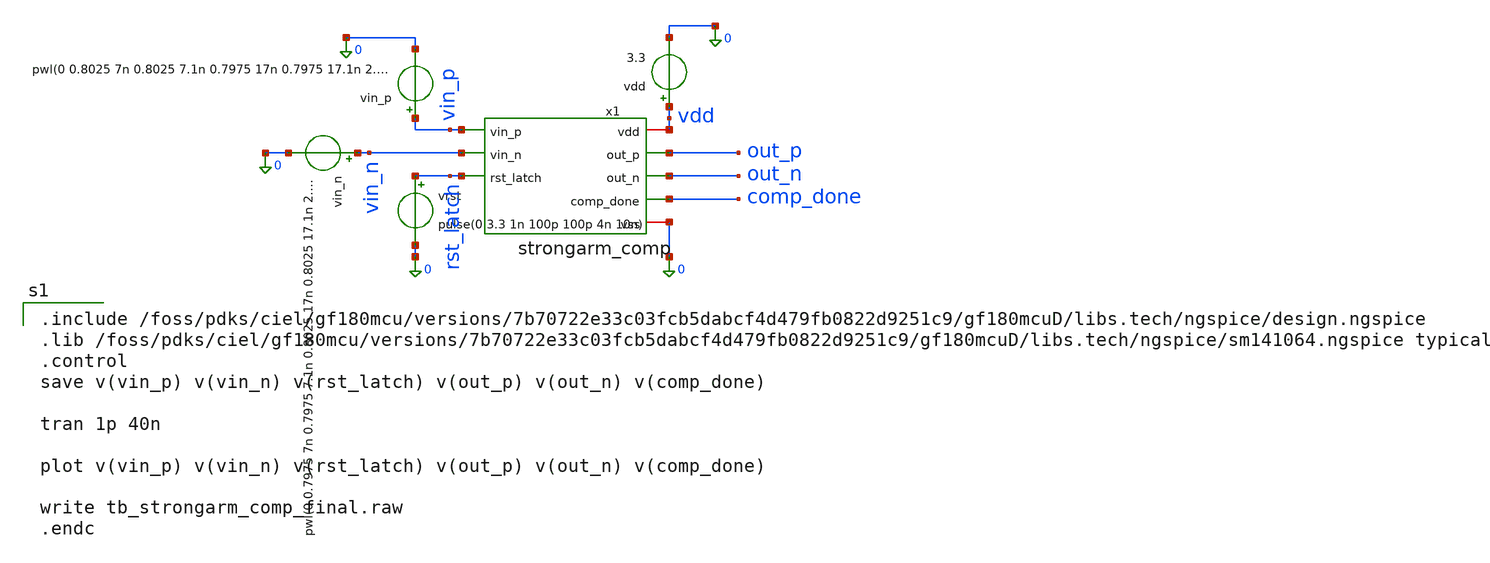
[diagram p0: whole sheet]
** sch_path: xschem/sar_adc/blocks/comparator/testbench/tb_strongarm_comp_final.sch
**.subckt tb_strongarm_comp_final
vdd vdd 0 3.3
vin_p vin_p 0 pwl(0 0.8025 7n 0.8025 7.1n 0.7975 17n 0.7975 17.1n 2.5025 27n 2.5025 27.1n 2.4975 40n
+ 2.4975)
vin_n vin_n 0 pwl(0 0.7975 7n 0.7975 7.1n 0.8025 17n 0.8025 17.1n 2.4975 27n 2.4975 27.1n 2.5025 40n
+ 2.5025)
vrst rst_latch 0 pulse(0 3.3 1n 100p 100p 4n 10n)
x1 vin_p vdd vin_n out_p rst_latch out_n 0 comp_done strongarm_comp
**** begin user architecture code

.include /foss/pdks/ciel/gf180mcu/versions/7b70722e33c03fcb5dabcf4d479fb0822d9251c9/gf180mcuD/libs.tech/ngspice/design.ngspice
.lib /foss/pdks/ciel/gf180mcu/versions/7b70722e33c03fcb5dabcf4d479fb0822d9251c9/gf180mcuD/libs.tech/ngspice/sm141064.ngspice typical
.control
save v(vin_p) v(vin_n) v(rst_latch) v(out_p) v(out_n) v(comp_done)

tran 1p 40n

plot v(vin_p) v(vin_n) v(rst_latch) v(out_p) v(out_n) v(comp_done)

write tb_strongarm_comp_final.raw
.endc

**** end user architecture code
**.ends

* expanding   symbol:  sar_adc/blocks/comparator/strongarm_comp.sym # of pins=8
** sym_path: xschem/sar_adc/blocks/comparator/strongarm_comp.sym
** sch_path: xschem/sar_adc/blocks/comparator/strongarm_comp.sch
.subckt strongarm_comp vin_p vdd vin_n out_p rst_latch out_n vss comp_done
*.ipin vin_p
*.ipin vin_n
*.ipin rst_latch
*.opin out_p
*.opin out_n
*.iopin vdd
*.iopin vss
*.opin comp_done
x1 vdd vin_p out_p vin_n out_n rst_latch vss strongarm_comp_core
x2 vdd out_n out_p done_evt vss comp_nand_3v3
x3 vdd done_evt done_d1 vss comp_inv_3v3
x4 vdd done_d1 comp_done vss comp_inv_3v3
.ends


* expanding   symbol:  sar_adc/blocks/comparator/strongarm_comp_core.sym # of pins=7
** sym_path: xschem/sar_adc/blocks/comparator/strongarm_comp_core.sym
** sch_path: xschem/sar_adc/blocks/comparator/strongarm_comp_core.sch
.subckt strongarm_comp_core vdd vin_p out_p vin_n out_n rst_latch vss
*.ipin vin_p
*.ipin vin_n
*.ipin rst_latch
*.iopin vdd
*.iopin vss
*.opin out_p
*.opin out_n
XMtail net1 rst_latch vss vss nfet_03v3 L=0.28u W=0.22u nf=1 ad='int((nf+1)/2) * W/nf * 0.18u' as='int((nf+2)/2) * W/nf * 0.18u'
+ pd='2*int((nf+1)/2) * (W/nf + 0.18u)' ps='2*int((nf+2)/2) * (W/nf + 0.18u)' nrd='0.18u / W' nrs='0.18u / W'
+ sa=0 sb=0 sd=0 m=1
XM1 net2 vin_p net1 vss nfet_03v3 L=0.28u W=0.22u nf=1 ad='int((nf+1)/2) * W/nf * 0.18u' as='int((nf+2)/2) * W/nf * 0.18u'
+ pd='2*int((nf+1)/2) * (W/nf + 0.18u)' ps='2*int((nf+2)/2) * (W/nf + 0.18u)' nrd='0.18u / W' nrs='0.18u / W'
+ sa=0 sb=0 sd=0 m=1
XM2 net3 vin_n net1 vss nfet_03v3 L=0.28u W=0.22u nf=1 ad='int((nf+1)/2) * W/nf * 0.18u' as='int((nf+2)/2) * W/nf * 0.18u'
+ pd='2*int((nf+1)/2) * (W/nf + 0.18u)' ps='2*int((nf+2)/2) * (W/nf + 0.18u)' nrd='0.18u / W' nrs='0.18u / W'
+ sa=0 sb=0 sd=0 m=1
XM3 out_p out_n net2 vss nfet_03v3 L=0.28u W=0.22u nf=1 ad='int((nf+1)/2) * W/nf * 0.18u' as='int((nf+2)/2) * W/nf * 0.18u'
+ pd='2*int((nf+1)/2) * (W/nf + 0.18u)' ps='2*int((nf+2)/2) * (W/nf + 0.18u)' nrd='0.18u / W' nrs='0.18u / W'
+ sa=0 sb=0 sd=0 m=1
XM4 out_n out_p net3 vss nfet_03v3 L=0.28u W=0.22u nf=1 ad='int((nf+1)/2) * W/nf * 0.18u' as='int((nf+2)/2) * W/nf * 0.18u'
+ pd='2*int((nf+1)/2) * (W/nf + 0.18u)' ps='2*int((nf+2)/2) * (W/nf + 0.18u)' nrd='0.18u / W' nrs='0.18u / W'
+ sa=0 sb=0 sd=0 m=1
XM5 out_p out_n vdd vdd pfet_03v3 L=0.28u W=0.22u nf=1 ad='int((nf+1)/2) * W/nf * 0.18u' as='int((nf+2)/2) * W/nf * 0.18u'
+ pd='2*int((nf+1)/2) * (W/nf + 0.18u)' ps='2*int((nf+2)/2) * (W/nf + 0.18u)' nrd='0.18u / W' nrs='0.18u / W'
+ sa=0 sb=0 sd=0 m=1
XM6 out_n out_p vdd vdd pfet_03v3 L=0.28u W=0.22u nf=1 ad='int((nf+1)/2) * W/nf * 0.18u' as='int((nf+2)/2) * W/nf * 0.18u'
+ pd='2*int((nf+1)/2) * (W/nf + 0.18u)' ps='2*int((nf+2)/2) * (W/nf + 0.18u)' nrd='0.18u / W' nrs='0.18u / W'
+ sa=0 sb=0 sd=0 m=1
XM7 out_p rst_latch vdd vdd pfet_03v3 L=0.28u W=0.22u nf=1 ad='int((nf+1)/2) * W/nf * 0.18u' as='int((nf+2)/2) * W/nf * 0.18u'
+ pd='2*int((nf+1)/2) * (W/nf + 0.18u)' ps='2*int((nf+2)/2) * (W/nf + 0.18u)' nrd='0.18u / W' nrs='0.18u / W'
+ sa=0 sb=0 sd=0 m=1
XM8 out_n rst_latch vdd vdd pfet_03v3 L=0.28u W=0.22u nf=1 ad='int((nf+1)/2) * W/nf * 0.18u' as='int((nf+2)/2) * W/nf * 0.18u'
+ pd='2*int((nf+1)/2) * (W/nf + 0.18u)' ps='2*int((nf+2)/2) * (W/nf + 0.18u)' nrd='0.18u / W' nrs='0.18u / W'
+ sa=0 sb=0 sd=0 m=1
XM9 net2 rst_latch vdd vdd pfet_03v3 L=0.28u W=0.22u nf=1 ad='int((nf+1)/2) * W/nf * 0.18u' as='int((nf+2)/2) * W/nf * 0.18u'
+ pd='2*int((nf+1)/2) * (W/nf + 0.18u)' ps='2*int((nf+2)/2) * (W/nf + 0.18u)' nrd='0.18u / W' nrs='0.18u / W'
+ sa=0 sb=0 sd=0 m=1
XM10 net3 rst_latch vdd vdd pfet_03v3 L=0.28u W=0.22u nf=1 ad='int((nf+1)/2) * W/nf * 0.18u' as='int((nf+2)/2) * W/nf * 0.18u'
+ pd='2*int((nf+1)/2) * (W/nf + 0.18u)' ps='2*int((nf+2)/2) * (W/nf + 0.18u)' nrd='0.18u / W' nrs='0.18u / W'
+ sa=0 sb=0 sd=0 m=1
.ends


* expanding   symbol:  sar_adc/blocks/comparator/comp_nand_3v3.sym # of pins=5
** sym_path: xschem/sar_adc/blocks/comparator/comp_nand_3v3.sym
** sch_path: xschem/sar_adc/blocks/comparator/comp_nand_3v3.sch
.subckt comp_nand_3v3 vdd b a y vss
*.iopin vdd
*.iopin vss
*.opin y
*.ipin a
*.ipin b
XM1 y a vdd vdd pfet_03v3 L=0.28u W=0.22u nf=1 ad='int((nf+1)/2) * W/nf * 0.18u' as='int((nf+2)/2) * W/nf * 0.18u'
+ pd='2*int((nf+1)/2) * (W/nf + 0.18u)' ps='2*int((nf+2)/2) * (W/nf + 0.18u)' nrd='0.18u / W' nrs='0.18u / W'
+ sa=0 sb=0 sd=0 m=1
XM2 y b vdd vdd pfet_03v3 L=0.28u W=0.22u nf=1 ad='int((nf+1)/2) * W/nf * 0.18u' as='int((nf+2)/2) * W/nf * 0.18u'
+ pd='2*int((nf+1)/2) * (W/nf + 0.18u)' ps='2*int((nf+2)/2) * (W/nf + 0.18u)' nrd='0.18u / W' nrs='0.18u / W'
+ sa=0 sb=0 sd=0 m=1
XM3 y a net1 vss nfet_03v3 L=0.28u W=0.22u nf=1 ad='int((nf+1)/2) * W/nf * 0.18u' as='int((nf+2)/2) * W/nf * 0.18u'
+ pd='2*int((nf+1)/2) * (W/nf + 0.18u)' ps='2*int((nf+2)/2) * (W/nf + 0.18u)' nrd='0.18u / W' nrs='0.18u / W'
+ sa=0 sb=0 sd=0 m=1
XM4 net1 b vss vss nfet_03v3 L=0.28u W=0.22u nf=1 ad='int((nf+1)/2) * W/nf * 0.18u' as='int((nf+2)/2) * W/nf * 0.18u'
+ pd='2*int((nf+1)/2) * (W/nf + 0.18u)' ps='2*int((nf+2)/2) * (W/nf + 0.18u)' nrd='0.18u / W' nrs='0.18u / W'
+ sa=0 sb=0 sd=0 m=1
.ends


* expanding   symbol:  sar_adc/blocks/comparator/comp_inv_3v3.sym # of pins=4
** sym_path: xschem/sar_adc/blocks/comparator/comp_inv_3v3.sym
** sch_path: xschem/sar_adc/blocks/comparator/comp_inv_3v3.sch
.subckt comp_inv_3v3 vdd vi vo vss
*.ipin vi
*.opin vo
*.iopin vdd
*.iopin vss
XM2 vo vi vdd vdd pfet_03v3 L=0.28u W=2u nf=1 ad='int((nf+1)/2) * W/nf * 0.18u' as='int((nf+2)/2) * W/nf * 0.18u'
+ pd='2*int((nf+1)/2) * (W/nf + 0.18u)' ps='2*int((nf+2)/2) * (W/nf + 0.18u)' nrd='0.18u / W' nrs='0.18u / W'
+ sa=0 sb=0 sd=0 m=1
XM1 vo vi vss vss nfet_03v3 L=0.28u W=1u nf=1 ad='int((nf+1)/2) * W/nf * 0.18u' as='int((nf+2)/2) * W/nf * 0.18u'
+ pd='2*int((nf+1)/2) * (W/nf + 0.18u)' ps='2*int((nf+2)/2) * (W/nf + 0.18u)' nrd='0.18u / W' nrs='0.18u / W'
+ sa=0 sb=0 sd=0 m=1
.ends

.end
